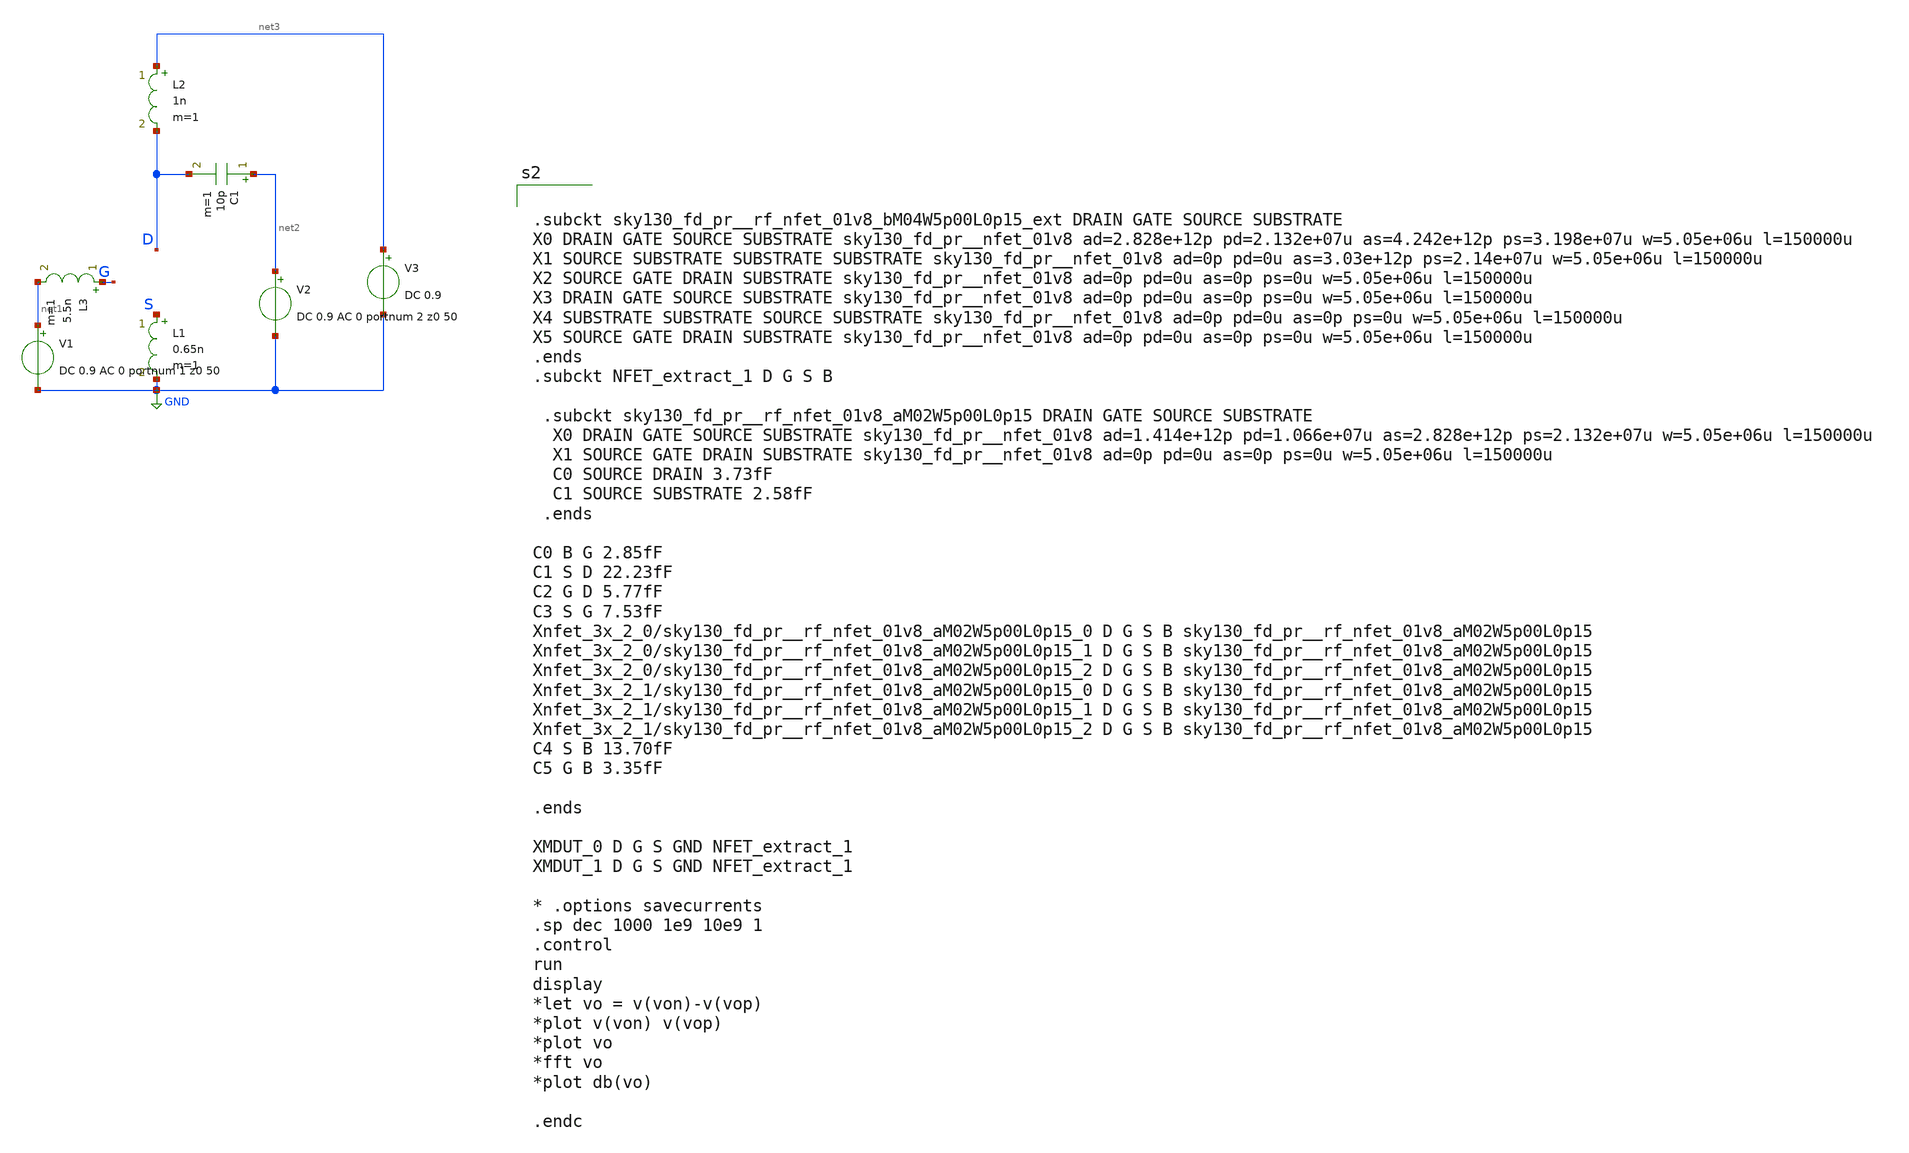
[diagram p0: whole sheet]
** sch_path: xschem/zp_test2.sch
**.subckt zp_test2
V2 net2 GND DC 0.9 AC 0 portnum 2 z0 50
V1 net1 GND DC 0.9 AC 0 portnum 1 z0 50
L1 S GND 0.65n m=1
C1 net2 D 10p m=1
L2 net3 D 1n m=1
V3 net3 GND DC 0.9
L3 G net1 5.5n m=1
**** begin user architecture code


.subckt sky130_fd_pr__rf_nfet_01v8_bM04W5p00L0p15_ext DRAIN GATE SOURCE SUBSTRATE
X0 DRAIN GATE SOURCE SUBSTRATE sky130_fd_pr__nfet_01v8 ad=2.828e+12p pd=2.132e+07u as=4.242e+12p
+ ps=3.198e+07u w=5.05e+06u l=150000u
X1 SOURCE SUBSTRATE SUBSTRATE SUBSTRATE sky130_fd_pr__nfet_01v8 ad=0p pd=0u as=3.03e+12p
+ ps=2.14e+07u w=5.05e+06u l=150000u
X2 SOURCE GATE DRAIN SUBSTRATE sky130_fd_pr__nfet_01v8 ad=0p pd=0u as=0p ps=0u w=5.05e+06u l=150000u
X3 DRAIN GATE SOURCE SUBSTRATE sky130_fd_pr__nfet_01v8 ad=0p pd=0u as=0p ps=0u w=5.05e+06u l=150000u
X4 SUBSTRATE SUBSTRATE SOURCE SUBSTRATE sky130_fd_pr__nfet_01v8 ad=0p pd=0u as=0p ps=0u w=5.05e+06u
+ l=150000u
X5 SOURCE GATE DRAIN SUBSTRATE sky130_fd_pr__nfet_01v8 ad=0p pd=0u as=0p ps=0u w=5.05e+06u l=150000u
.ends
.subckt NFET_extract_1 D G S B

 .subckt sky130_fd_pr__rf_nfet_01v8_aM02W5p00L0p15 DRAIN GATE SOURCE SUBSTRATE
  X0 DRAIN GATE SOURCE SUBSTRATE sky130_fd_pr__nfet_01v8 ad=1.414e+12p pd=1.066e+07u as=2.828e+12p
+ ps=2.132e+07u w=5.05e+06u l=150000u
  X1 SOURCE GATE DRAIN SUBSTRATE sky130_fd_pr__nfet_01v8 ad=0p pd=0u as=0p ps=0u w=5.05e+06u
+ l=150000u
  C0 SOURCE DRAIN 3.73fF
  C1 SOURCE SUBSTRATE 2.58fF
 .ends

C0 B G 2.85fF
C1 S D 22.23fF
C2 G D 5.77fF
C3 S G 7.53fF
Xnfet_3x_2_0/sky130_fd_pr__rf_nfet_01v8_aM02W5p00L0p15_0 D G S B
+ sky130_fd_pr__rf_nfet_01v8_aM02W5p00L0p15
Xnfet_3x_2_0/sky130_fd_pr__rf_nfet_01v8_aM02W5p00L0p15_1 D G S B
+ sky130_fd_pr__rf_nfet_01v8_aM02W5p00L0p15
Xnfet_3x_2_0/sky130_fd_pr__rf_nfet_01v8_aM02W5p00L0p15_2 D G S B
+ sky130_fd_pr__rf_nfet_01v8_aM02W5p00L0p15
Xnfet_3x_2_1/sky130_fd_pr__rf_nfet_01v8_aM02W5p00L0p15_0 D G S B
+ sky130_fd_pr__rf_nfet_01v8_aM02W5p00L0p15
Xnfet_3x_2_1/sky130_fd_pr__rf_nfet_01v8_aM02W5p00L0p15_1 D G S B
+ sky130_fd_pr__rf_nfet_01v8_aM02W5p00L0p15
Xnfet_3x_2_1/sky130_fd_pr__rf_nfet_01v8_aM02W5p00L0p15_2 D G S B
+ sky130_fd_pr__rf_nfet_01v8_aM02W5p00L0p15
C4 S B 13.70fF
C5 G B 3.35fF

.ends

XMDUT_0 D G S GND NFET_extract_1
XMDUT_1 D G S GND NFET_extract_1

* .options savecurrents
.sp dec 1000 1e9 10e9 1
.control
run
display
*let vo = v(von)-v(vop)
*plot v(von) v(vop)
*plot vo
*fft vo
*plot db(vo)

.endc


.lib $::SKYWATER_MODELS/sky130.lib.spice tt
* .include $::PDKPATH/libs.ref/sky130_fd_sc_hvl/spice/sky130_fd_sc_hvl.spice

**** end user architecture code
**.ends
.GLOBAL GND
.end
